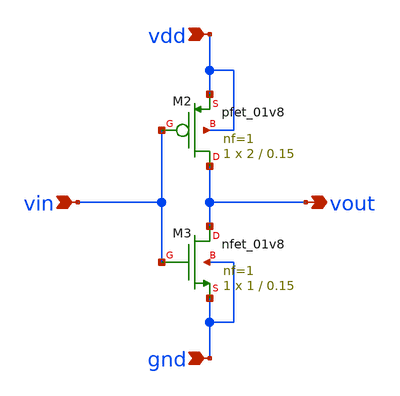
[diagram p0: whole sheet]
** sch_path: VLSI/VLSI_TEST_06/inv_vtc.sch
**.subckt inv_vtc vin vout vdd gnd
*.ipin vin
*.opin vout
*.ipin vdd
*.ipin gnd
XM2 vout vin vdd vdd sky130_fd_pr__pfet_01v8 L=0.15 W=2 nf=1 ad='int((nf+1)/2) * W/nf * 0.29' as='int((nf+2)/2) * W/nf * 0.29'
+ pd='2*int((nf+1)/2) * (W/nf + 0.29)' ps='2*int((nf+2)/2) * (W/nf + 0.29)' nrd='0.29 / W' nrs='0.29 / W'
+ sa=0 sb=0 sd=0 mult=1 m=1
XM3 vout vin gnd gnd sky130_fd_pr__nfet_01v8 L=0.15 W=1 nf=1 ad='int((nf+1)/2) * W/nf * 0.29' as='int((nf+2)/2) * W/nf * 0.29'
+ pd='2*int((nf+1)/2) * (W/nf + 0.29)' ps='2*int((nf+2)/2) * (W/nf + 0.29)' nrd='0.29 / W' nrs='0.29 / W'
+ sa=0 sb=0 sd=0 mult=1 m=1
**.ends
.end
